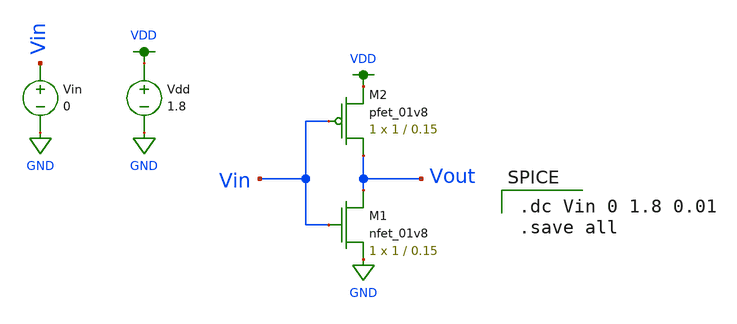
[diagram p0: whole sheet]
** sch_path: mp1/inverter/cmos_inverter_vtc.sch
**.subckt cmos_inverter_vtc
XM2 Vout Vin VDD VDD sky130_fd_pr__pfet_01v8 L=0.15 W=1 nf=1 ad='int((nf+1)/2) * W/nf * 0.29' as='int((nf+2)/2) * W/nf * 0.29'
+ pd='2*int((nf+1)/2) * (W/nf + 0.29)' ps='2*int((nf+2)/2) * (W/nf + 0.29)' nrd='0.29 / W' nrs='0.29 / W'
+ sa=0 sb=0 sd=0 mult=1 m=1
Vdd VDD GND 1.8
Vin Vin GND 0
XM1 Vout Vin GND GND sky130_fd_pr__nfet_01v8 L=0.15 W=1 nf=1 ad='int((nf+1)/2) * W/nf * 0.29' as='int((nf+2)/2) * W/nf * 0.29'
+ pd='2*int((nf+1)/2) * (W/nf + 0.29)' ps='2*int((nf+2)/2) * (W/nf + 0.29)' nrd='0.29 / W' nrs='0.29 / W'
+ sa=0 sb=0 sd=0 mult=1 m=1
**** begin user architecture code

.option wnflag=1
.lib ~/skywater/skywater-pdk/libraries/sky130_fd_pr_ngspice/latest/models/sky130.lib.spice tt


.dc Vin 0 1.8 0.01
.save all

**** end user architecture code
**.ends
.GLOBAL VDD
.GLOBAL GND
.end
